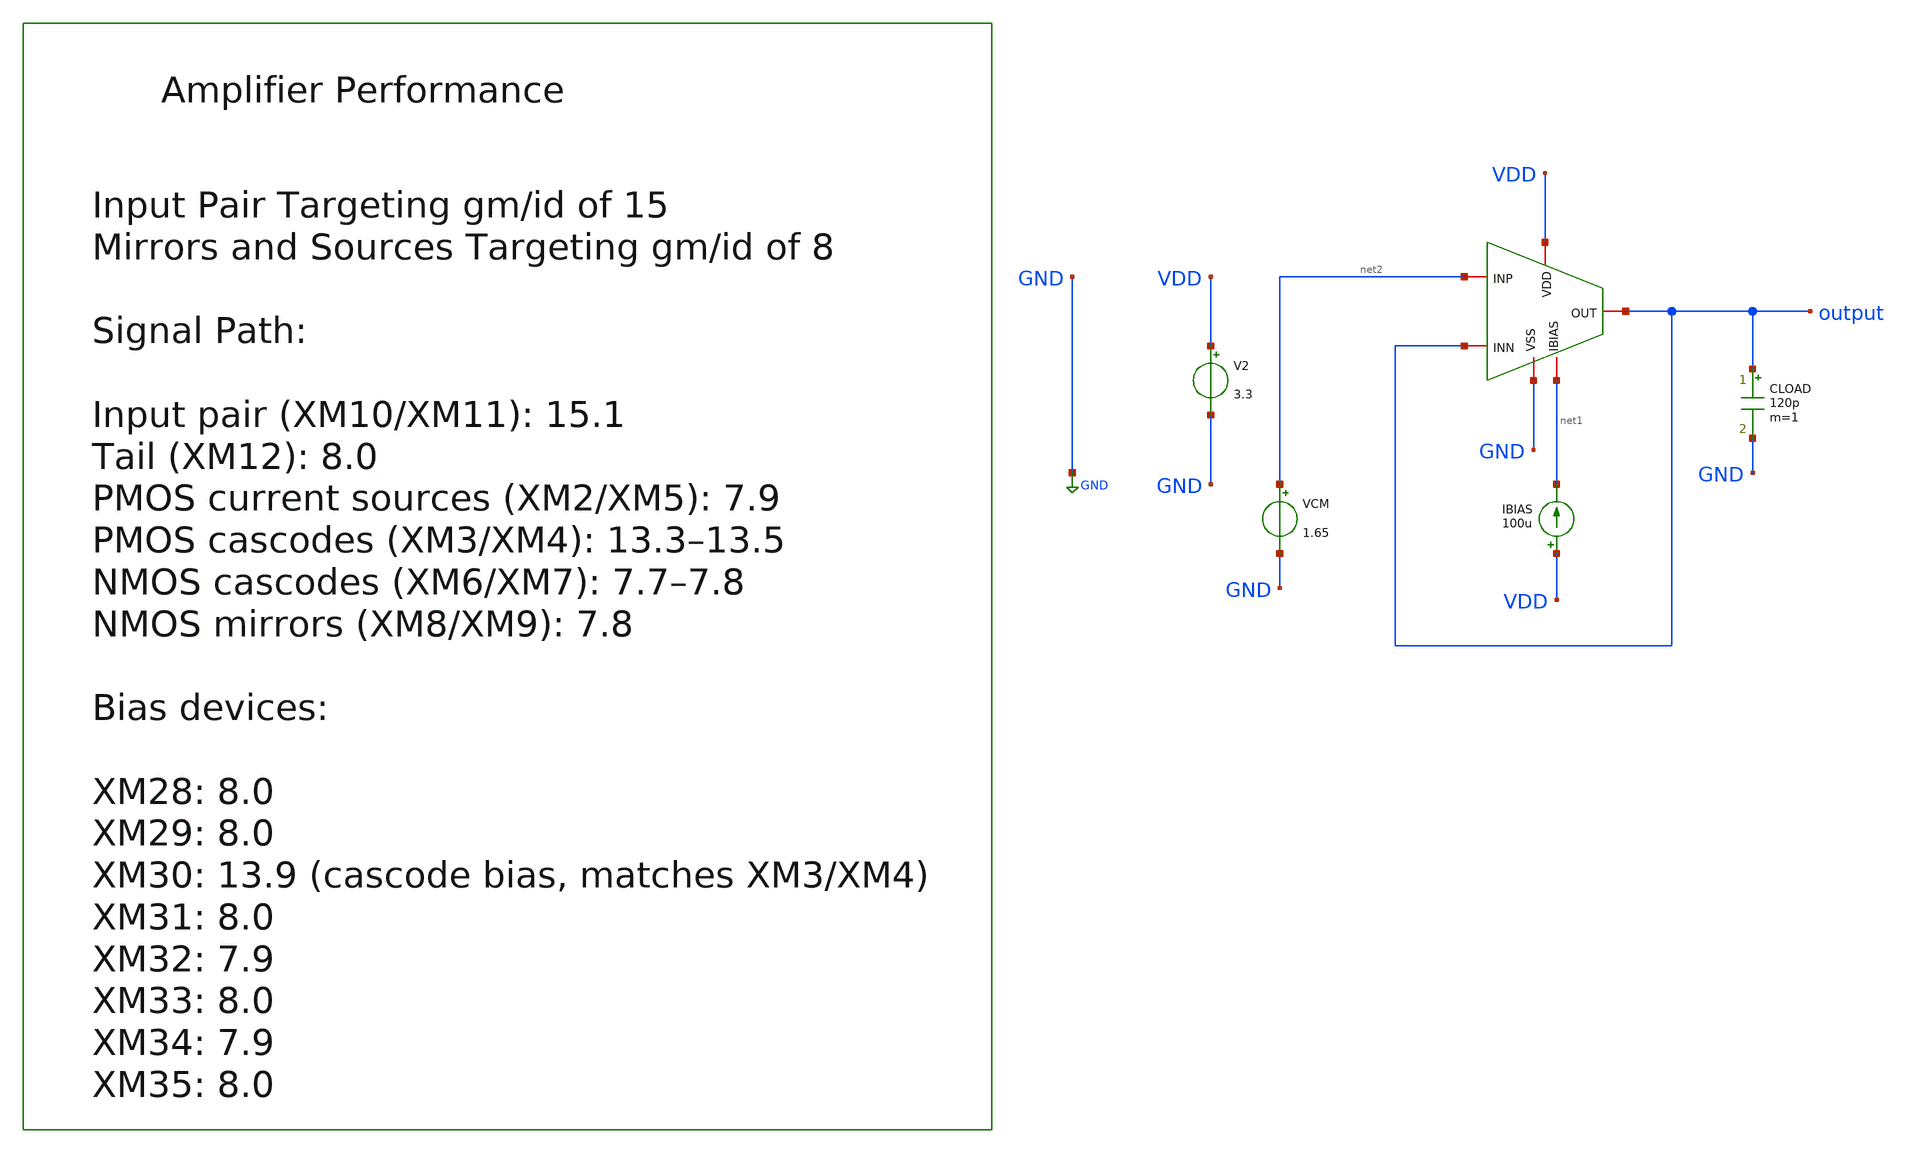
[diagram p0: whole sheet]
** sch_path: designs/libs/core_amps/ota_folded_cascode/tb/op_gmid_tb.sch
**.subckt op_gmid_tb
IBIAS VDD net1 100u
V2 VDD GND 3.3
CLOAD output GND 120p m=1
VCM net2 GND 1.65
x1 VDD GND output net2 output net1 ota_folded_cascode
**** begin user architecture code

.include $::180MCU_MODELS/design.ngspice
.lib $::180MCU_MODELS/sm141064.ngspice typical



.control
op

let gmid_xm28 = @m.x1.xm28.m0[gm]/@m.x1.xm28.m0[id]
let gmid_xm33 = @m.x1.xm33.m0[gm]/@m.x1.xm33.m0[id]
let gmid_xm32 = @m.x1.xm32.m0[gm]/@m.x1.xm32.m0[id]
let gmid_xm29 = @m.x1.xm29.m0[gm]/@m.x1.xm29.m0[id]
let gmid_xm30 = @m.x1.xm30.m0[gm]/@m.x1.xm30.m0[id]
let gmid_xm31 = @m.x1.xm31.m0[gm]/@m.x1.xm31.m0[id]
let gmid_xm34 = @m.x1.xm34.m0[gm]/@m.x1.xm34.m0[id]
let gmid_xm35 = @m.x1.xm35.m0[gm]/@m.x1.xm35.m0[id]
let gmid_xm11 = @m.x1.xm11.m0[gm]/@m.x1.xm11.m0[id]
let gmid_xm10 = @m.x1.xm10.m0[gm]/@m.x1.xm10.m0[id]
let gmid_xm12 = @m.x1.xm12.m0[gm]/@m.x1.xm12.m0[id]
let gmid_xm2  = @m.x1.xm2.m0[gm]/@m.x1.xm2.m0[id]
let gmid_xm3  = @m.x1.xm3.m0[gm]/@m.x1.xm3.m0[id]
let gmid_xm4  = @m.x1.xm4.m0[gm]/@m.x1.xm4.m0[id]
let gmid_xm5  = @m.x1.xm5.m0[gm]/@m.x1.xm5.m0[id]
let gmid_xm6  = @m.x1.xm6.m0[gm]/@m.x1.xm6.m0[id]
let gmid_xm7  = @m.x1.xm7.m0[gm]/@m.x1.xm7.m0[id]
let gmid_xm8  = @m.x1.xm8.m0[gm]/@m.x1.xm8.m0[id]
let gmid_xm9  = @m.x1.xm9.m0[gm]/@m.x1.xm9.m0[id]
print gmid_xm28 gmid_xm33 gmid_xm32 gmid_xm29
print gmid_xm30 gmid_xm31 gmid_xm34 gmid_xm35
print gmid_xm11 gmid_xm10 gmid_xm12
print gmid_xm2 gmid_xm3 gmid_xm4 gmid_xm5
print gmid_xm6 gmid_xm7 gmid_xm8 gmid_xm9

.endc


**** end user architecture code
**.ends
.GLOBAL GND
.end
